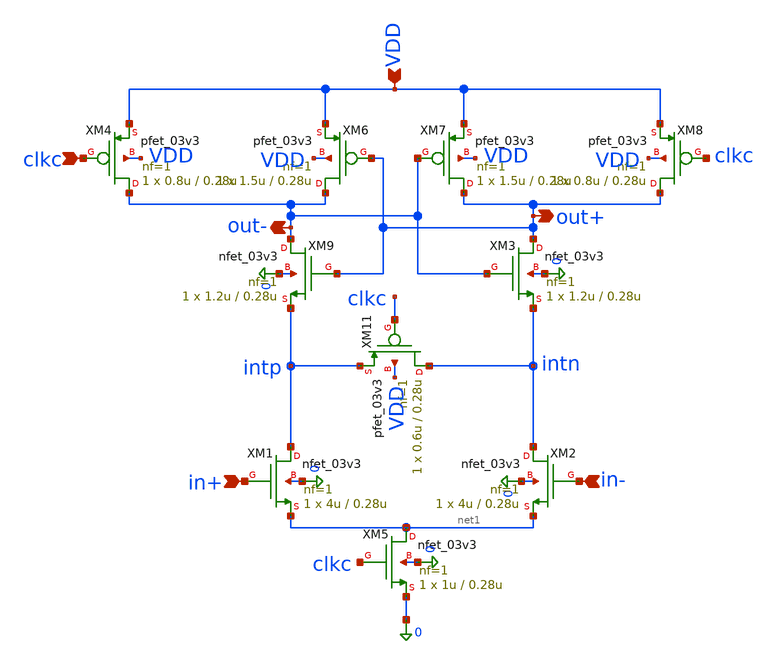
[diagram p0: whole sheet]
** sch_path: Design_Files/IC Design/Schematic/SAR_ADC_BLOCKS/SA_LATCH/SA_LATCH.sch
**.subckt SA_LATCH VDD out+ out- clkc in+ in-
*.ipin VDD
*.opin out+
*.opin out-
*.ipin clkc
*.ipin in+
*.ipin in-
XM1 intp in+ net1 0 nfet_03v3 L=0.28u W=4u nf=1 ad='int((nf+1)/2) * W/nf * 0.18u' as='int((nf+2)/2) * W/nf * 0.18u'
+ pd='2*int((nf+1)/2) * (W/nf + 0.18u)' ps='2*int((nf+2)/2) * (W/nf + 0.18u)' nrd='0.18u / W' nrs='0.18u / W'
+ sa=0 sb=0 sd=0 m=1
XM3 out+ out- intn 0 nfet_03v3 L=0.28u W=1.2u nf=1 ad='int((nf+1)/2) * W/nf * 0.18u' as='int((nf+2)/2) * W/nf * 0.18u'
+ pd='2*int((nf+1)/2) * (W/nf + 0.18u)' ps='2*int((nf+2)/2) * (W/nf + 0.18u)' nrd='0.18u / W' nrs='0.18u / W'
+ sa=0 sb=0 sd=0 m=1
XM5 net1 clkc 0 0 nfet_03v3 L=0.28u W=1u nf=1 ad='int((nf+1)/2) * W/nf * 0.18u' as='int((nf+2)/2) * W/nf * 0.18u'
+ pd='2*int((nf+1)/2) * (W/nf + 0.18u)' ps='2*int((nf+2)/2) * (W/nf + 0.18u)' nrd='0.18u / W' nrs='0.18u / W'
+ sa=0 sb=0 sd=0 m=1
XM7 out+ out- VDD VDD pfet_03v3 L=0.28u W=1.5u nf=1 ad='int((nf+1)/2) * W/nf * 0.18u' as='int((nf+2)/2) * W/nf * 0.18u'
+ pd='2*int((nf+1)/2) * (W/nf + 0.18u)' ps='2*int((nf+2)/2) * (W/nf + 0.18u)' nrd='0.18u / W' nrs='0.18u / W'
+ sa=0 sb=0 sd=0 m=1
XM4 out- clkc VDD VDD pfet_03v3 L=0.28u W=0.8u nf=1 ad='int((nf+1)/2) * W/nf * 0.18u' as='int((nf+2)/2) * W/nf * 0.18u'
+ pd='2*int((nf+1)/2) * (W/nf + 0.18u)' ps='2*int((nf+2)/2) * (W/nf + 0.18u)' nrd='0.18u / W' nrs='0.18u / W'
+ sa=0 sb=0 sd=0 m=1
XM6 out- out+ VDD VDD pfet_03v3 L=0.28u W=1.5u nf=1 ad='int((nf+1)/2) * W/nf * 0.18u' as='int((nf+2)/2) * W/nf * 0.18u'
+ pd='2*int((nf+1)/2) * (W/nf + 0.18u)' ps='2*int((nf+2)/2) * (W/nf + 0.18u)' nrd='0.18u / W' nrs='0.18u / W'
+ sa=0 sb=0 sd=0 m=1
XM8 out+ clkc VDD VDD pfet_03v3 L=0.28u W=0.8u nf=1 ad='int((nf+1)/2) * W/nf * 0.18u' as='int((nf+2)/2) * W/nf * 0.18u'
+ pd='2*int((nf+1)/2) * (W/nf + 0.18u)' ps='2*int((nf+2)/2) * (W/nf + 0.18u)' nrd='0.18u / W' nrs='0.18u / W'
+ sa=0 sb=0 sd=0 m=1
XM9 out- out+ intp 0 nfet_03v3 L=0.28u W=1.2u nf=1 ad='int((nf+1)/2) * W/nf * 0.18u' as='int((nf+2)/2) * W/nf * 0.18u'
+ pd='2*int((nf+1)/2) * (W/nf + 0.18u)' ps='2*int((nf+2)/2) * (W/nf + 0.18u)' nrd='0.18u / W' nrs='0.18u / W'
+ sa=0 sb=0 sd=0 m=1
XM2 intn in- net1 0 nfet_03v3 L=0.28u W=4u nf=1 ad='int((nf+1)/2) * W/nf * 0.18u' as='int((nf+2)/2) * W/nf * 0.18u'
+ pd='2*int((nf+1)/2) * (W/nf + 0.18u)' ps='2*int((nf+2)/2) * (W/nf + 0.18u)' nrd='0.18u / W' nrs='0.18u / W'
+ sa=0 sb=0 sd=0 m=1
XM11 intn clkc intp VDD pfet_03v3 L=0.28u W=0.6u nf=1 ad='int((nf+1)/2) * W/nf * 0.18u' as='int((nf+2)/2) * W/nf * 0.18u'
+ pd='2*int((nf+1)/2) * (W/nf + 0.18u)' ps='2*int((nf+2)/2) * (W/nf + 0.18u)' nrd='0.18u / W' nrs='0.18u / W'
+ sa=0 sb=0 sd=0 m=1
**.ends
.end
